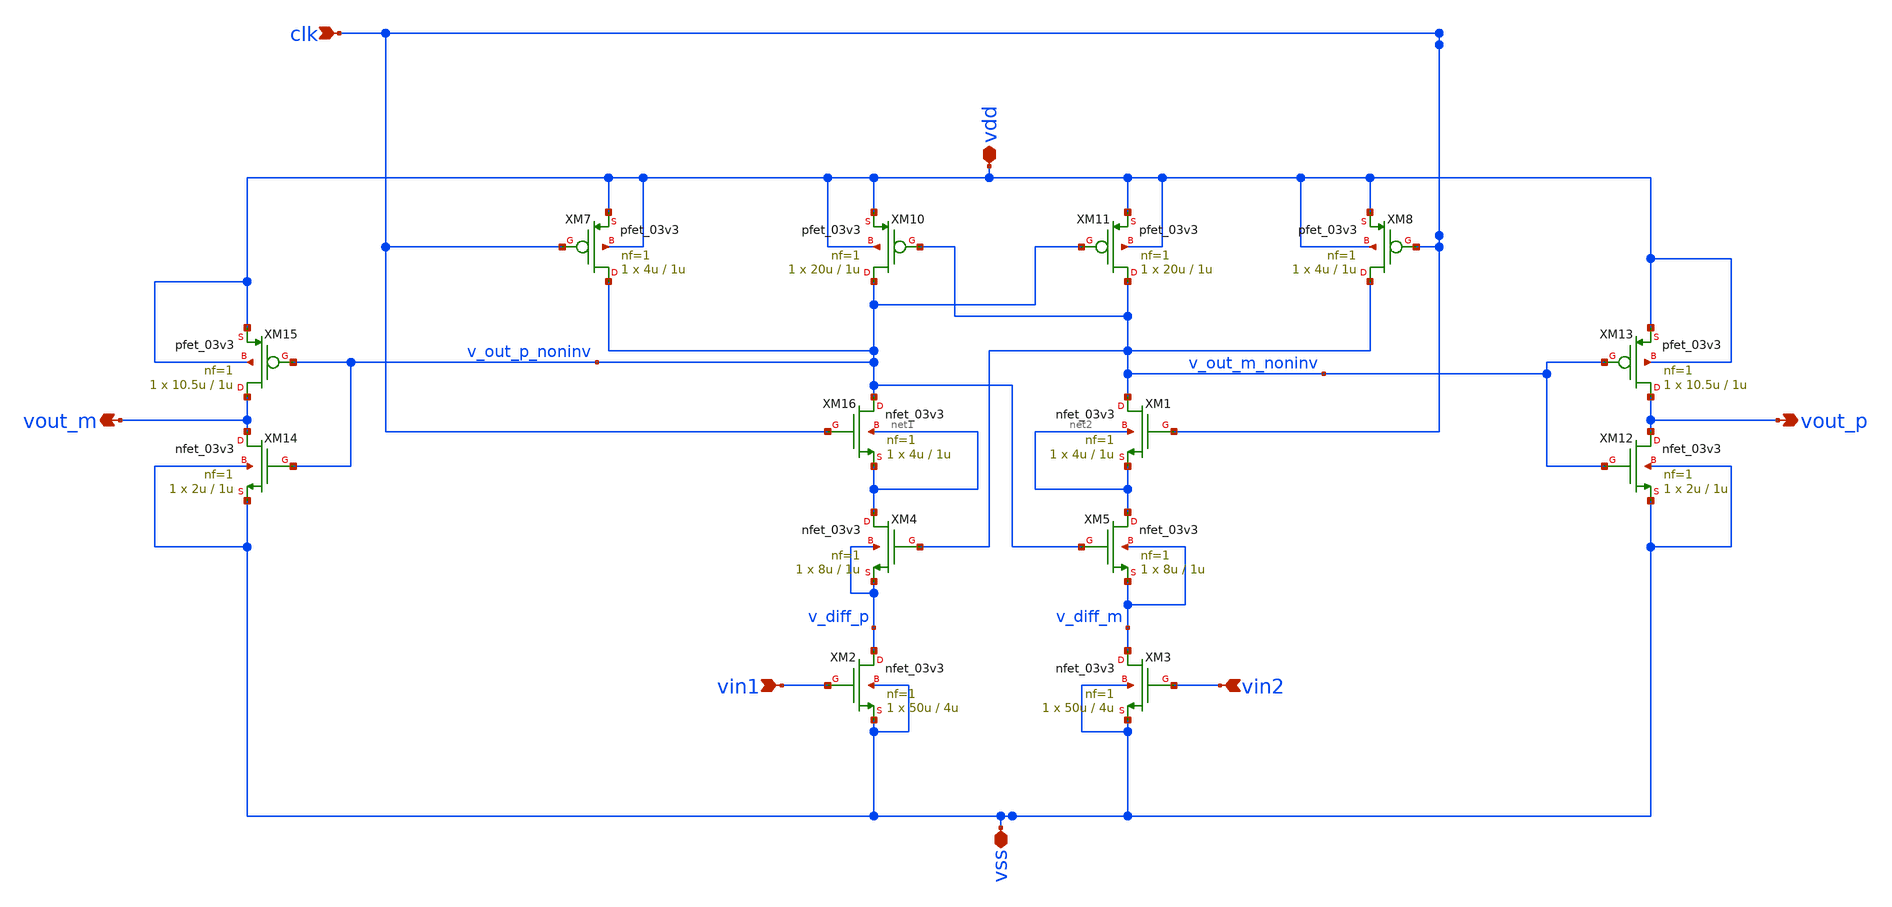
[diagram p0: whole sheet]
** sch_path: General/ADC/Comparator/Comparator_v2.sch
**.subckt Comparator_v2 vdd vss clk vin1 vin2 vout_p vout_m
*.iopin vdd
*.iopin vss
*.ipin clk
*.ipin vin1
*.ipin vin2
*.opin vout_p
*.opin vout_m
XM1 v_out_m_noninv clk net2 net2 nfet_03v3 L=1u W=4u nf=1 ad='int((nf+1)/2) * W/nf * 0.18u' as='int((nf+2)/2) * W/nf * 0.18u'
+ pd='2*int((nf+1)/2) * (W/nf + 0.18u)' ps='2*int((nf+2)/2) * (W/nf + 0.18u)' nrd='0.18u / W' nrs='0.18u / W'
+ sa=0 sb=0 sd=0 m=1
XM2 v_diff_p vin1 vss vss nfet_03v3 L=4u W=50u nf=1 ad='int((nf+1)/2) * W/nf * 0.18u' as='int((nf+2)/2) * W/nf * 0.18u'
+ pd='2*int((nf+1)/2) * (W/nf + 0.18u)' ps='2*int((nf+2)/2) * (W/nf + 0.18u)' nrd='0.18u / W' nrs='0.18u / W'
+ sa=0 sb=0 sd=0 m=1
XM3 v_diff_m vin2 vss vss nfet_03v3 L=4u W=50u nf=1 ad='int((nf+1)/2) * W/nf * 0.18u' as='int((nf+2)/2) * W/nf * 0.18u'
+ pd='2*int((nf+1)/2) * (W/nf + 0.18u)' ps='2*int((nf+2)/2) * (W/nf + 0.18u)' nrd='0.18u / W' nrs='0.18u / W'
+ sa=0 sb=0 sd=0 m=1
XM4 net1 v_out_m_noninv v_diff_p v_diff_p nfet_03v3 L=1u W=8u nf=1 ad='int((nf+1)/2) * W/nf * 0.18u'
+ as='int((nf+2)/2) * W/nf * 0.18u' pd='2*int((nf+1)/2) * (W/nf + 0.18u)' ps='2*int((nf+2)/2) * (W/nf + 0.18u)'
+ nrd='0.18u / W' nrs='0.18u / W' sa=0 sb=0 sd=0 m=1
XM5 net2 v_out_p_noninv v_diff_m v_diff_m nfet_03v3 L=1u W=8u nf=1 ad='int((nf+1)/2) * W/nf * 0.18u'
+ as='int((nf+2)/2) * W/nf * 0.18u' pd='2*int((nf+1)/2) * (W/nf + 0.18u)' ps='2*int((nf+2)/2) * (W/nf + 0.18u)'
+ nrd='0.18u / W' nrs='0.18u / W' sa=0 sb=0 sd=0 m=1
XM7 v_out_p_noninv clk vdd vdd pfet_03v3 L=1u W=4u nf=1 ad='int((nf+1)/2) * W/nf * 0.18u' as='int((nf+2)/2) * W/nf * 0.18u'
+ pd='2*int((nf+1)/2) * (W/nf + 0.18u)' ps='2*int((nf+2)/2) * (W/nf + 0.18u)' nrd='0.18u / W' nrs='0.18u / W'
+ sa=0 sb=0 sd=0 m=1
XM8 v_out_m_noninv clk vdd vdd pfet_03v3 L=1u W=4u nf=1 ad='int((nf+1)/2) * W/nf * 0.18u' as='int((nf+2)/2) * W/nf * 0.18u'
+ pd='2*int((nf+1)/2) * (W/nf + 0.18u)' ps='2*int((nf+2)/2) * (W/nf + 0.18u)' nrd='0.18u / W' nrs='0.18u / W'
+ sa=0 sb=0 sd=0 m=1
XM10 v_out_p_noninv v_out_m_noninv vdd vdd pfet_03v3 L=1u W=20u nf=1 ad='int((nf+1)/2) * W/nf * 0.18u'
+ as='int((nf+2)/2) * W/nf * 0.18u' pd='2*int((nf+1)/2) * (W/nf + 0.18u)' ps='2*int((nf+2)/2) * (W/nf + 0.18u)'
+ nrd='0.18u / W' nrs='0.18u / W' sa=0 sb=0 sd=0 m=1
XM11 v_out_m_noninv v_out_p_noninv vdd vdd pfet_03v3 L=1u W=20u nf=1 ad='int((nf+1)/2) * W/nf * 0.18u'
+ as='int((nf+2)/2) * W/nf * 0.18u' pd='2*int((nf+1)/2) * (W/nf + 0.18u)' ps='2*int((nf+2)/2) * (W/nf + 0.18u)'
+ nrd='0.18u / W' nrs='0.18u / W' sa=0 sb=0 sd=0 m=1
XM12 vout_p v_out_m_noninv vss vss nfet_03v3 L=1u W=2u nf=1 ad='int((nf+1)/2) * W/nf * 0.18u' as='int((nf+2)/2) * W/nf * 0.18u'
+ pd='2*int((nf+1)/2) * (W/nf + 0.18u)' ps='2*int((nf+2)/2) * (W/nf + 0.18u)' nrd='0.18u / W' nrs='0.18u / W'
+ sa=0 sb=0 sd=0 m=1
XM13 vout_p v_out_m_noninv vdd vdd pfet_03v3 L=1u W=10.5u nf=1 ad='int((nf+1)/2) * W/nf * 0.18u' as='int((nf+2)/2) * W/nf * 0.18u'
+ pd='2*int((nf+1)/2) * (W/nf + 0.18u)' ps='2*int((nf+2)/2) * (W/nf + 0.18u)' nrd='0.18u / W' nrs='0.18u / W'
+ sa=0 sb=0 sd=0 m=1
XM14 vout_m v_out_p_noninv vss vss nfet_03v3 L=1u W=2u nf=1 ad='int((nf+1)/2) * W/nf * 0.18u' as='int((nf+2)/2) * W/nf * 0.18u'
+ pd='2*int((nf+1)/2) * (W/nf + 0.18u)' ps='2*int((nf+2)/2) * (W/nf + 0.18u)' nrd='0.18u / W' nrs='0.18u / W'
+ sa=0 sb=0 sd=0 m=1
XM15 vout_m v_out_p_noninv vdd vdd pfet_03v3 L=1u W=10.5u nf=1 ad='int((nf+1)/2) * W/nf * 0.18u' as='int((nf+2)/2) * W/nf * 0.18u'
+ pd='2*int((nf+1)/2) * (W/nf + 0.18u)' ps='2*int((nf+2)/2) * (W/nf + 0.18u)' nrd='0.18u / W' nrs='0.18u / W'
+ sa=0 sb=0 sd=0 m=1
XM16 v_out_p_noninv clk net1 net1 nfet_03v3 L=1u W=4u nf=1 ad='int((nf+1)/2) * W/nf * 0.18u' as='int((nf+2)/2) * W/nf * 0.18u'
+ pd='2*int((nf+1)/2) * (W/nf + 0.18u)' ps='2*int((nf+2)/2) * (W/nf + 0.18u)' nrd='0.18u / W' nrs='0.18u / W'
+ sa=0 sb=0 sd=0 m=1
**.ends
.end
